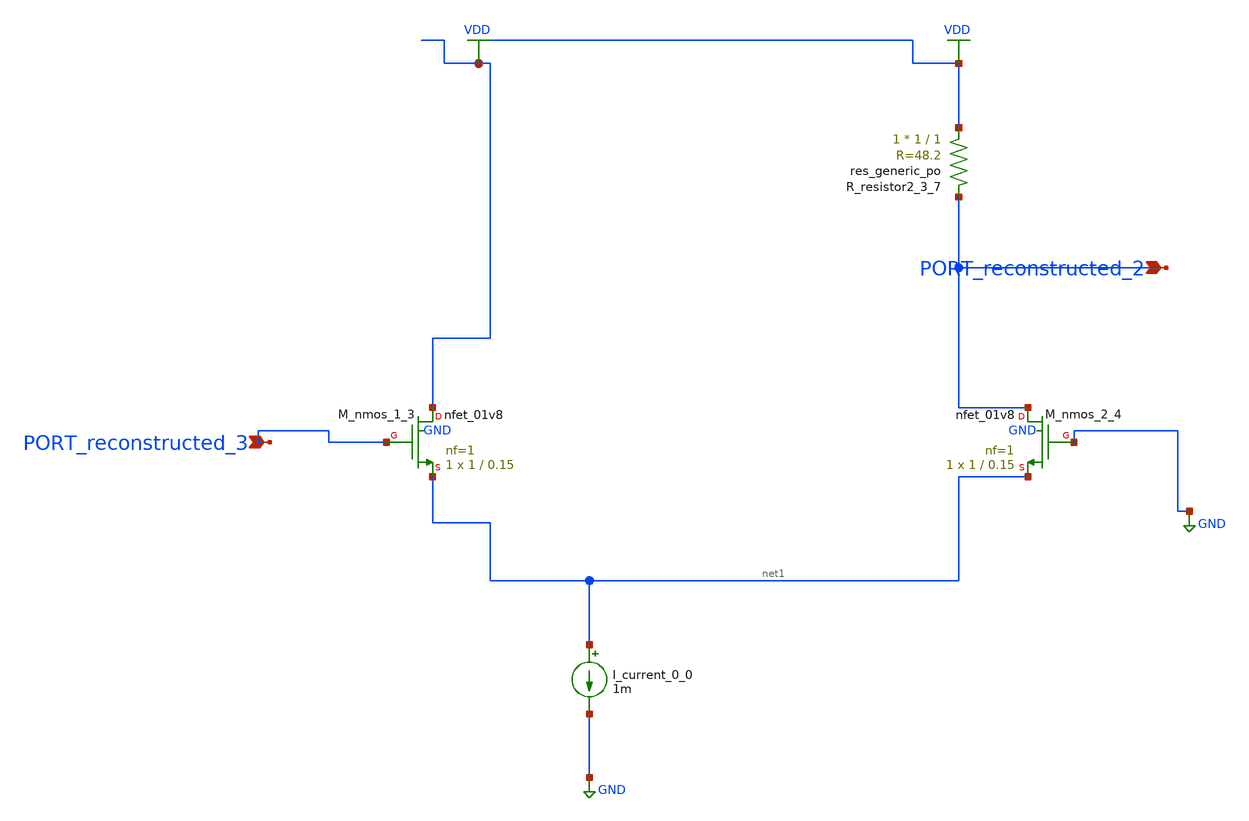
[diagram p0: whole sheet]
** sch_path: schematics/AMSNet/272.sch
**.subckt 272 PORT_reconstructed_2 PORT_reconstructed_3
*.ipin PORT_reconstructed_2
*.ipin PORT_reconstructed_3
I_current_0_0 net1 GND 1m
XM_nmos_1_3 VDD PORT_reconstructed_3 net1 GND sky130_fd_pr__nfet_01v8 L=0.15 W=1 nf=1 ad='int((1 + 1)/2) * 1 / 1 * 0.29'
+ as='int((1 + 2)/2) * 1 / 1 * 0.29' pd='2*int((1 + 1)/2) * (1 / 1 + 0.29)' ps='2*int((1 + 2)/2) * (1 / 1 + 0.29)'
+ nrd='0.29 / 1 ' nrs='0.29 / 1 ' sa=0 sb=0 sd=0 mult=1 m=1
XM_nmos_2_4 PORT_reconstructed_2 GND net1 GND sky130_fd_pr__nfet_01v8 L=0.15 W=1 nf=1 ad='int((1 + 1)/2) * 1 / 1 * 0.29'
+ as='int((1 + 2)/2) * 1 / 1 * 0.29' pd='2*int((1 + 1)/2) * (1 / 1 + 0.29)' ps='2*int((1 + 2)/2) * (1 / 1 + 0.29)'
+ nrd='0.29 / 1 ' nrs='0.29 / 1 ' sa=0 sb=0 sd=0 mult=1 m=1
XR_resistor2_3_7 VDD PORT_reconstructed_2 sky130_fd_pr__res_generic_po W=1 L=1 m=1
**.ends
.GLOBAL GND
.GLOBAL VDD
.end
